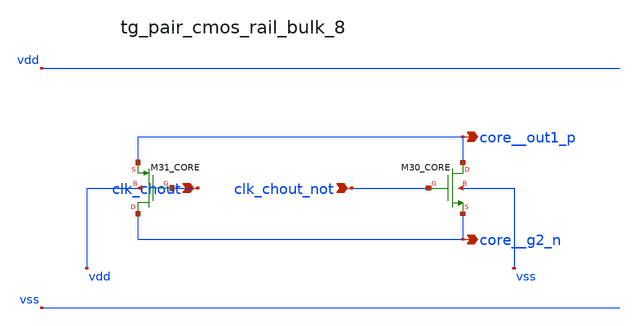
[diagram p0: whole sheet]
** sch_path: analog-db/raw/ia_006_fan_chopper_cmfb/hier/blocks/tg_pair_cmos_rail_bulk_8.sch
**.subckt tg_pair_cmos_rail_bulk_8 clk_chout clk_chout_not core__out1_p core__g2_n
*.ipin clk_chout
*.ipin clk_chout_not
*.opin core__out1_p
*.opin core__g2_n
XM30_CORE core__out1_p clk_chout_not core__g2_n vss sg13_lv_nmos w=x_dut_xm30_core_w
+ l=x_dut_xm30_core_l ng=1 m=x_dut_xm30_core_m
XM31_CORE core__g2_n clk_chout core__out1_p vdd sg13_lv_pmos w=x_dut_xm31_core_w l=x_dut_xm31_core_l
+ ng=1 m=x_dut_xm31_core_m
**.ends
.end
